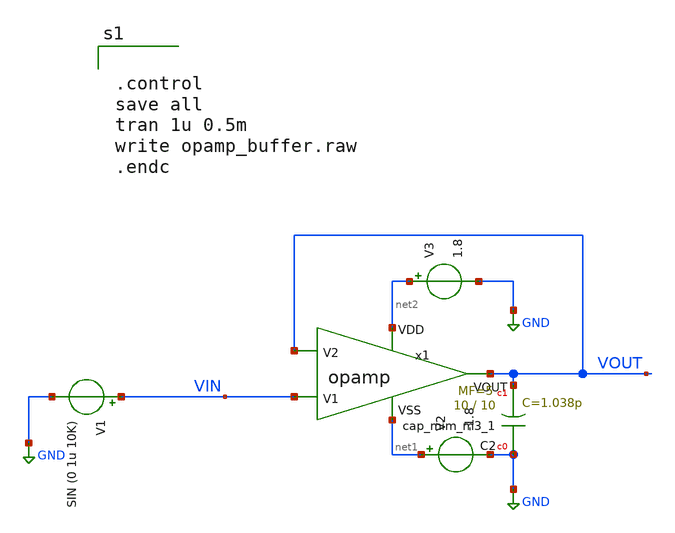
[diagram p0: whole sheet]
** sch_path: opamp_buffer.sch
**.subckt opamp_buffer
V3 net2 GND 1.8
V2 net1 GND -1.8
x1 net2 net1 VIN VOUT VOUT opamp
V1 VIN GND SIN (0 1u 10K)
XC2 GND VOUT sky130_fd_pr__cap_mim_m3_1 W=10 L=10 MF=5 m=5
**** begin user architecture code

** opencircuitdesign pdks install
.lib $::SKYWATER_MODELS/sky130.lib.spice tt




.control
save all
tran 1u 0.5m
write opamp_buffer.raw
.endc


**** end user architecture code
**.ends

* expanding   symbol:  /home/caonam/OpenLane/FINALPROJECT/sky130_hcmus_ip__instramp/xschem/opamp.sym
*+ # of pins=5
** sym_path: /home/caonam/OpenLane/FINALPROJECT/sky130_hcmus_ip__instramp/xschem/opamp.sym
** sch_path: /home/caonam/OpenLane/FINALPROJECT/sky130_hcmus_ip__instramp/xschem/opamp.sch
.subckt opamp VDD VSS V1 V2 VOUT
*.ipin VSS
*.ipin VDD
*.ipin V2
*.ipin V1
*.opin VOUT
XM2 net2 V2 net1 VSS sky130_fd_pr__nfet_g5v0d10v5 L=1 W=17.45 nf=1 ad='int((nf+1)/2) * W/nf * 0.29' as='int((nf+2)/2) * W/nf * 0.29'
+ pd='2*int((nf+1)/2) * (W/nf + 0.29)' ps='2*int((nf+2)/2) * (W/nf + 0.29)' nrd='0.29 / W' nrs='0.29 / W'
+ sa=0 sb=0 sd=0 mult=1 m=1
XM1 net3 net2 VDD VDD sky130_fd_pr__pfet_g5v0d10v5 L=1 W=30 nf=1 ad='int((nf+1)/2) * W/nf * 0.29' as='int((nf+2)/2) * W/nf * 0.29'
+ pd='2*int((nf+1)/2) * (W/nf + 0.29)' ps='2*int((nf+2)/2) * (W/nf + 0.29)' nrd='0.29 / W' nrs='0.29 / W'
+ sa=0 sb=0 sd=0 mult=1 m=1
XM4 net3 V1 net1 VSS sky130_fd_pr__nfet_g5v0d10v5 L=1 W=17.45 nf=1 ad='int((nf+1)/2) * W/nf * 0.29' as='int((nf+2)/2) * W/nf * 0.29'
+ pd='2*int((nf+1)/2) * (W/nf + 0.29)' ps='2*int((nf+2)/2) * (W/nf + 0.29)' nrd='0.29 / W' nrs='0.29 / W'
+ sa=0 sb=0 sd=0 mult=1 m=1
XM5 net6 net4 VSS VSS sky130_fd_pr__nfet_g5v0d10v5 L=1 W=15.17 nf=1 ad='int((nf+1)/2) * W/nf * 0.29'
+ as='int((nf+2)/2) * W/nf * 0.29' pd='2*int((nf+1)/2) * (W/nf + 0.29)' ps='2*int((nf+2)/2) * (W/nf + 0.29)'
+ nrd='0.29 / W' nrs='0.29 / W' sa=0 sb=0 sd=0 mult=1 m=1
XM6 net8 net4 VSS VSS sky130_fd_pr__nfet_g5v0d10v5 L=1 W=19 nf=1 ad='int((nf+1)/2) * W/nf * 0.29' as='int((nf+2)/2) * W/nf * 0.29'
+ pd='2*int((nf+1)/2) * (W/nf + 0.29)' ps='2*int((nf+2)/2) * (W/nf + 0.29)' nrd='0.29 / W' nrs='0.29 / W'
+ sa=0 sb=0 sd=0 mult=1 m=1
XM7 net4 net4 VSS VSS sky130_fd_pr__nfet_g5v0d10v5 L=1 W=15.17 nf=1 ad='int((nf+1)/2) * W/nf * 0.29'
+ as='int((nf+2)/2) * W/nf * 0.29' pd='2*int((nf+1)/2) * (W/nf + 0.29)' ps='2*int((nf+2)/2) * (W/nf + 0.29)'
+ nrd='0.29 / W' nrs='0.29 / W' sa=0 sb=0 sd=0 mult=1 m=1
XM3 net2 net2 VDD VDD sky130_fd_pr__pfet_g5v0d10v5 L=1 W=30 nf=1 ad='int((nf+1)/2) * W/nf * 0.29' as='int((nf+2)/2) * W/nf * 0.29'
+ pd='2*int((nf+1)/2) * (W/nf + 0.29)' ps='2*int((nf+2)/2) * (W/nf + 0.29)' nrd='0.29 / W' nrs='0.29 / W'
+ sa=0 sb=0 sd=0 mult=1 m=1
XM8 VOUT net3 VDD VDD sky130_fd_pr__pfet_g5v0d10v5 L=1 W=38 nf=1 ad='int((nf+1)/2) * W/nf * 0.29' as='int((nf+2)/2) * W/nf * 0.29'
+ pd='2*int((nf+1)/2) * (W/nf + 0.29)' ps='2*int((nf+2)/2) * (W/nf + 0.29)' nrd='0.29 / W' nrs='0.29 / W'
+ sa=0 sb=0 sd=0 mult=2 m=2
XC1 net5 net3 sky130_fd_pr__cap_mim_m3_1 W=9 L=9 MF=2 m=2
V_ibias net7 net4 0
.save i(v_ibias)
XR3 net5 VOUT VSS sky130_fd_pr__res_high_po_0p69 L=3.2 mult=1 m=1
V_ibias1 net1 net6 0
.save i(v_ibias1)
I1 net9 net10 63.26u
V_iout VOUT net8 0
.save i(v_iout)
XM9 VDD VDD net7 VSS sky130_fd_pr__nfet_g5v0d10v5 L=1 W=0.69 nf=1 ad='int((nf+1)/2) * W/nf * 0.29' as='int((nf+2)/2) * W/nf * 0.29'
+ pd='2*int((nf+1)/2) * (W/nf + 0.29)' ps='2*int((nf+2)/2) * (W/nf + 0.29)' nrd='0.29 / W' nrs='0.29 / W'
+ sa=0 sb=0 sd=0 mult=1 m=1
.ends

.GLOBAL GND
.end
